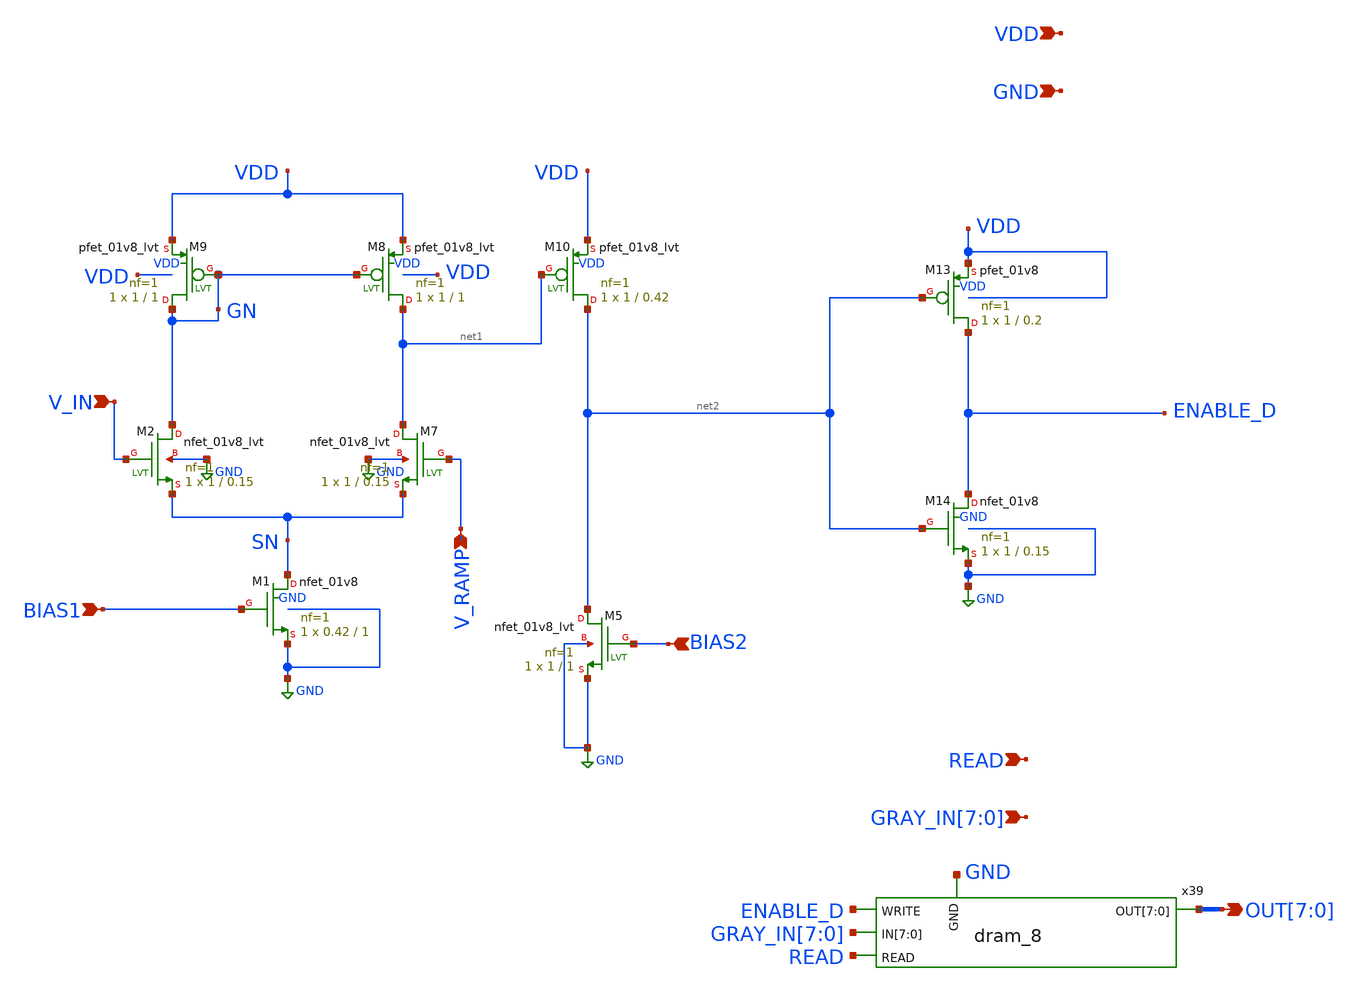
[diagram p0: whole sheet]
** sch_path: xschem/adc/8bit_adc.sch
**.subckt 8bit_adc VDD READ
*+ GRAY_IN[7],GRAY_IN[6],GRAY_IN[5],GRAY_IN[4],GRAY_IN[3],GRAY_IN[2],GRAY_IN[1],GRAY_IN[0] V_RAMP V_IN BIAS1 BIAS2 OUT[7],OUT[6],OUT[5],OUT[4],OUT[3],OUT[2],OUT[1],OUT[0] GND
*.ipin VDD
*.ipin READ
*.ipin GRAY_IN[7],GRAY_IN[6],GRAY_IN[5],GRAY_IN[4],GRAY_IN[3],GRAY_IN[2],GRAY_IN[1],GRAY_IN[0]
*.ipin V_RAMP
*.ipin V_IN
*.ipin BIAS1
*.ipin BIAS2
*.opin OUT[7],OUT[6],OUT[5],OUT[4],OUT[3],OUT[2],OUT[1],OUT[0]
*.ipin GND
XM2 GN V_IN SN GND sky130_fd_pr__nfet_01v8_lvt L=0.15 W=1 nf=1 ad='int((nf+1)/2) * W/nf * 0.29' as='int((nf+2)/2) * W/nf * 0.29'
+ pd='2*int((nf+1)/2) * (W/nf + 0.29)' ps='2*int((nf+2)/2) * (W/nf + 0.29)' nrd='0.29 / W' nrs='0.29 / W'
+ sa=0 sb=0 sd=0 mult=1 m=1
XM7 net1 V_RAMP SN GND sky130_fd_pr__nfet_01v8_lvt L=0.15 W=1 nf=1 ad='int((nf+1)/2) * W/nf * 0.29' as='int((nf+2)/2) * W/nf * 0.29'
+ pd='2*int((nf+1)/2) * (W/nf + 0.29)' ps='2*int((nf+2)/2) * (W/nf + 0.29)' nrd='0.29 / W' nrs='0.29 / W'
+ sa=0 sb=0 sd=0 mult=1 m=1
XM8 net1 GN VDD VDD sky130_fd_pr__pfet_01v8_lvt L=1 W=1 nf=1 ad='int((nf+1)/2) * W/nf * 0.29' as='int((nf+2)/2) * W/nf * 0.29'
+ pd='2*int((nf+1)/2) * (W/nf + 0.29)' ps='2*int((nf+2)/2) * (W/nf + 0.29)' nrd='0.29 / W' nrs='0.29 / W'
+ sa=0 sb=0 sd=0 mult=1 m=1
XM9 GN GN VDD VDD sky130_fd_pr__pfet_01v8_lvt L=1 W=1 nf=1 ad='int((nf+1)/2) * W/nf * 0.29' as='int((nf+2)/2) * W/nf * 0.29'
+ pd='2*int((nf+1)/2) * (W/nf + 0.29)' ps='2*int((nf+2)/2) * (W/nf + 0.29)' nrd='0.29 / W' nrs='0.29 / W'
+ sa=0 sb=0 sd=0 mult=1 m=1
XM10 net2 net1 VDD VDD sky130_fd_pr__pfet_01v8_lvt L=0.42 W=1 nf=1 ad='int((nf+1)/2) * W/nf * 0.29' as='int((nf+2)/2) * W/nf * 0.29'
+ pd='2*int((nf+1)/2) * (W/nf + 0.29)' ps='2*int((nf+2)/2) * (W/nf + 0.29)' nrd='0.29 / W' nrs='0.29 / W'
+ sa=0 sb=0 sd=0 mult=1 m=1
XM13 ENABLE_D net2 VDD VDD sky130_fd_pr__pfet_01v8 L=0.2 W=1 nf=1 ad='int((nf+1)/2) * W/nf * 0.29' as='int((nf+2)/2) * W/nf * 0.29'
+ pd='2*int((nf+1)/2) * (W/nf + 0.29)' ps='2*int((nf+2)/2) * (W/nf + 0.29)' nrd='0.29 / W' nrs='0.29 / W'
+ sa=0 sb=0 sd=0 mult=1 m=1
XM14 ENABLE_D net2 GND GND sky130_fd_pr__nfet_01v8 L=0.15 W=1 nf=1 ad='int((nf+1)/2) * W/nf * 0.29' as='int((nf+2)/2) * W/nf * 0.29'
+ pd='2*int((nf+1)/2) * (W/nf + 0.29)' ps='2*int((nf+2)/2) * (W/nf + 0.29)' nrd='0.29 / W' nrs='0.29 / W'
+ sa=0 sb=0 sd=0 mult=1 m=1
XM1 SN BIAS1 GND GND sky130_fd_pr__nfet_01v8 L=1 W=0.42 nf=1 ad='int((nf+1)/2) * W/nf * 0.29' as='int((nf+2)/2) * W/nf * 0.29'
+ pd='2*int((nf+1)/2) * (W/nf + 0.29)' ps='2*int((nf+2)/2) * (W/nf + 0.29)' nrd='0.29 / W' nrs='0.29 / W'
+ sa=0 sb=0 sd=0 mult=1 m=1
XM5 net2 BIAS2 GND GND sky130_fd_pr__nfet_01v8_lvt L=1 W=1 nf=1 ad='int((nf+1)/2) * W/nf * 0.29' as='int((nf+2)/2) * W/nf * 0.29'
+ pd='2*int((nf+1)/2) * (W/nf + 0.29)' ps='2*int((nf+2)/2) * (W/nf + 0.29)' nrd='0.29 / W' nrs='0.29 / W'
+ sa=0 sb=0 sd=0 mult=1 m=1
x39 OUT[7] OUT[6] OUT[5] OUT[4] OUT[3] OUT[2] OUT[1] OUT[0] ENABLE_D GRAY_IN[7] GRAY_IN[6]
+ GRAY_IN[5] GRAY_IN[4] GRAY_IN[3] GRAY_IN[2] GRAY_IN[1] GRAY_IN[0] READ GND dram_8
**.ends

* expanding   symbol:  digital_prims/dram_8.sym # of pins=5
** sym_path: xschem/digital_prims/dram_8.sym
** sch_path: xschem/digital_prims/dram_8.sch
.subckt dram_8 OUT[7] OUT[6] OUT[5] OUT[4] OUT[3] OUT[2] OUT[1] OUT[0] WRITE IN[7] IN[6] IN[5] IN[4]
+ IN[3] IN[2] IN[1] IN[0] READ GND
*.opin OUT[7],OUT[6],OUT[5],OUT[4],OUT[3],OUT[2],OUT[1],OUT[0]
*.ipin WRITE
*.ipin IN[7],IN[6],IN[5],IN[4],IN[3],IN[2],IN[1],IN[0]
*.ipin READ
*.ipin GND
x5 WRITE OUT[7] net1 IN[7] READ GND dram
x6 WRITE OUT[6] net2 IN[6] READ GND dram
x7 WRITE OUT[5] net3 IN[5] READ GND dram
x25 WRITE OUT[4] net4 IN[4] READ GND dram
x26 WRITE OUT[3] net5 IN[3] READ GND dram
x27 WRITE OUT[2] net6 IN[2] READ GND dram
x33 WRITE OUT[1] net7 IN[0] READ GND dram
x34 WRITE OUT[0] net8 IN[1] READ GND dram
.ends


* expanding   symbol:  digital_prims/dram.sym # of pins=6
** sym_path: xschem/digital_prims/dram.sym
** sch_path: xschem/digital_prims/dram.sch
.subckt dram WWL RBL storage WBL RWL GND
*.opin RBL
*.ipin RWL
*.ipin WBL
*.ipin WWL
*.opin storage
*.ipin GND
XM3 RWL storage RBL GND sky130_fd_pr__nfet_01v8 L=0.15 W=1 nf=1 ad='int((nf+1)/2) * W/nf * 0.29' as='int((nf+2)/2) * W/nf * 0.29'
+ pd='2*int((nf+1)/2) * (W/nf + 0.29)' ps='2*int((nf+2)/2) * (W/nf + 0.29)' nrd='0.29 / W' nrs='0.29 / W'
+ sa=0 sb=0 sd=0 mult=1 m=1
XM1 WBL WWL storage GND sky130_fd_pr__nfet_01v8 L=0.15 W=1 nf=1 ad='int((nf+1)/2) * W/nf * 0.29' as='int((nf+2)/2) * W/nf * 0.29'
+ pd='2*int((nf+1)/2) * (W/nf + 0.29)' ps='2*int((nf+2)/2) * (W/nf + 0.29)' nrd='0.29 / W' nrs='0.29 / W'
+ sa=0 sb=0 sd=0 mult=1 m=1
.ends

.GLOBAL GND
.end
